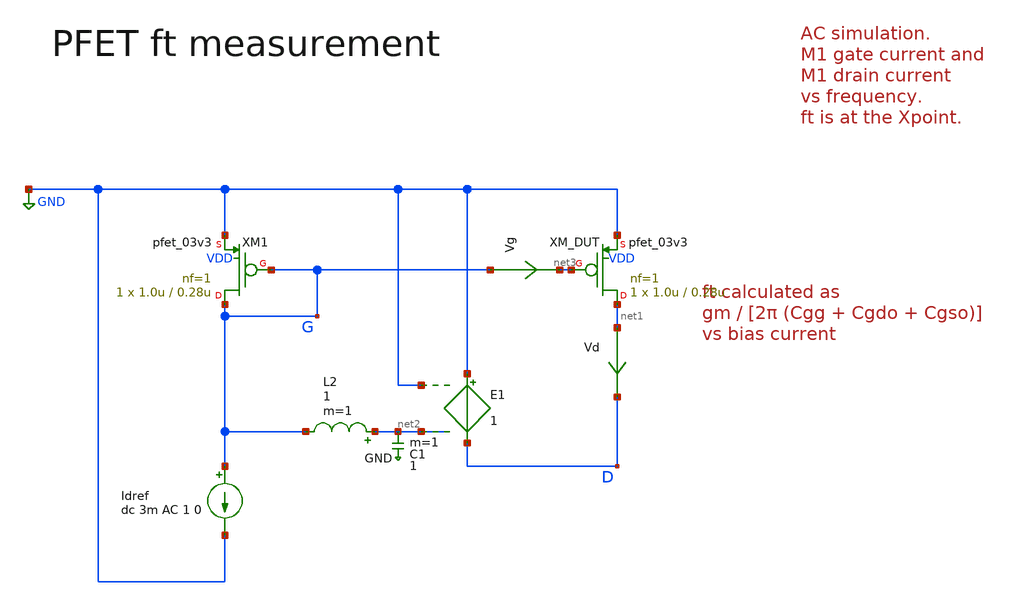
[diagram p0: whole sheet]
** sch_path: xschem/pfet_3v3_tb.sch
**.subckt pfet_3v3_tb
Idref G GND dc 3m AC 1 0
Vd net1 D 0
.save i(vd)
Vg G net3 0
.save i(vg)
L2 net2 G 1 m=1
C1 net2 GND 1 m=1
E1 GND D GND net2 1
XM_DUT net1 net3 GND VDD pfet_03v3 L=0.28u W=1.0u nf=1 ad='int((nf+1)/2) * W/nf * 0.18u' as='int((nf+2)/2) * W/nf * 0.18u'
+ pd='2*int((nf+1)/2) * (W/nf + 0.18u)' ps='2*int((nf+2)/2) * (W/nf + 0.18u)' nrd='0.18u / W' nrs='0.18u / W'
+ sa=0 sb=0 sd=0 m=1 par=1
XM1 G G GND VDD pfet_03v3 L=0.28u W=1.0u nf=1 ad='int((nf+1)/2) * W/nf * 0.18u' as='int((nf+2)/2) * W/nf * 0.18u'
+ pd='2*int((nf+1)/2) * (W/nf + 0.18u)' ps='2*int((nf+2)/2) * (W/nf + 0.18u)' nrd='0.18u / W' nrs='0.18u / W'
+ sa=0 sb=0 sd=0 m=1 par=1
**** begin user architecture code


.param mc_mm_switch=0
.include pfet_3v3_tb.save
.options filetype=ascii
* .option savecurrents
.save all
.control
* dc Idref 0.1e-3 10e-3 0.1e-3
let n_idx = 59
let start_iref = 0.1e-3
let stop_iref = 6e-3
let delta_iref = (stop_iref - start_iref) / n_idx
let iref_act = start_iref
let idx = 0
*loop
while iref_act le stop_iref
  alter idref iref_act
  op
  let gm = @m.xm_dut.m0[gm]
  let ids = @m.xm_dut.m0[id]
  let cgg =  @m.xm_dut.m0[cgg]
  let cgso =  @m.xm_dut.m0[cgso]
  let cgdo =  @m.xm_dut.m0[cgdo]
  let ft = gm/(2*pi*(cgg + cgso + cgdo))

  setscale iref_act
  settype current iref_act
  write pfet_3v3_tb.raw
  set appendwrite

  let iref_act = iref_act + delta_iref
  let idx = idx + 1
end

ac dec 10 1k 100G
remzerovec
write pfet_3v3_tb.raw

.endc
.end



.include $::180MCU_MODELS/design.ngspice
.lib $::180MCU_MODELS/sm141064.ngspice typical

**** end user architecture code
**.ends
.GLOBAL GND
.end
